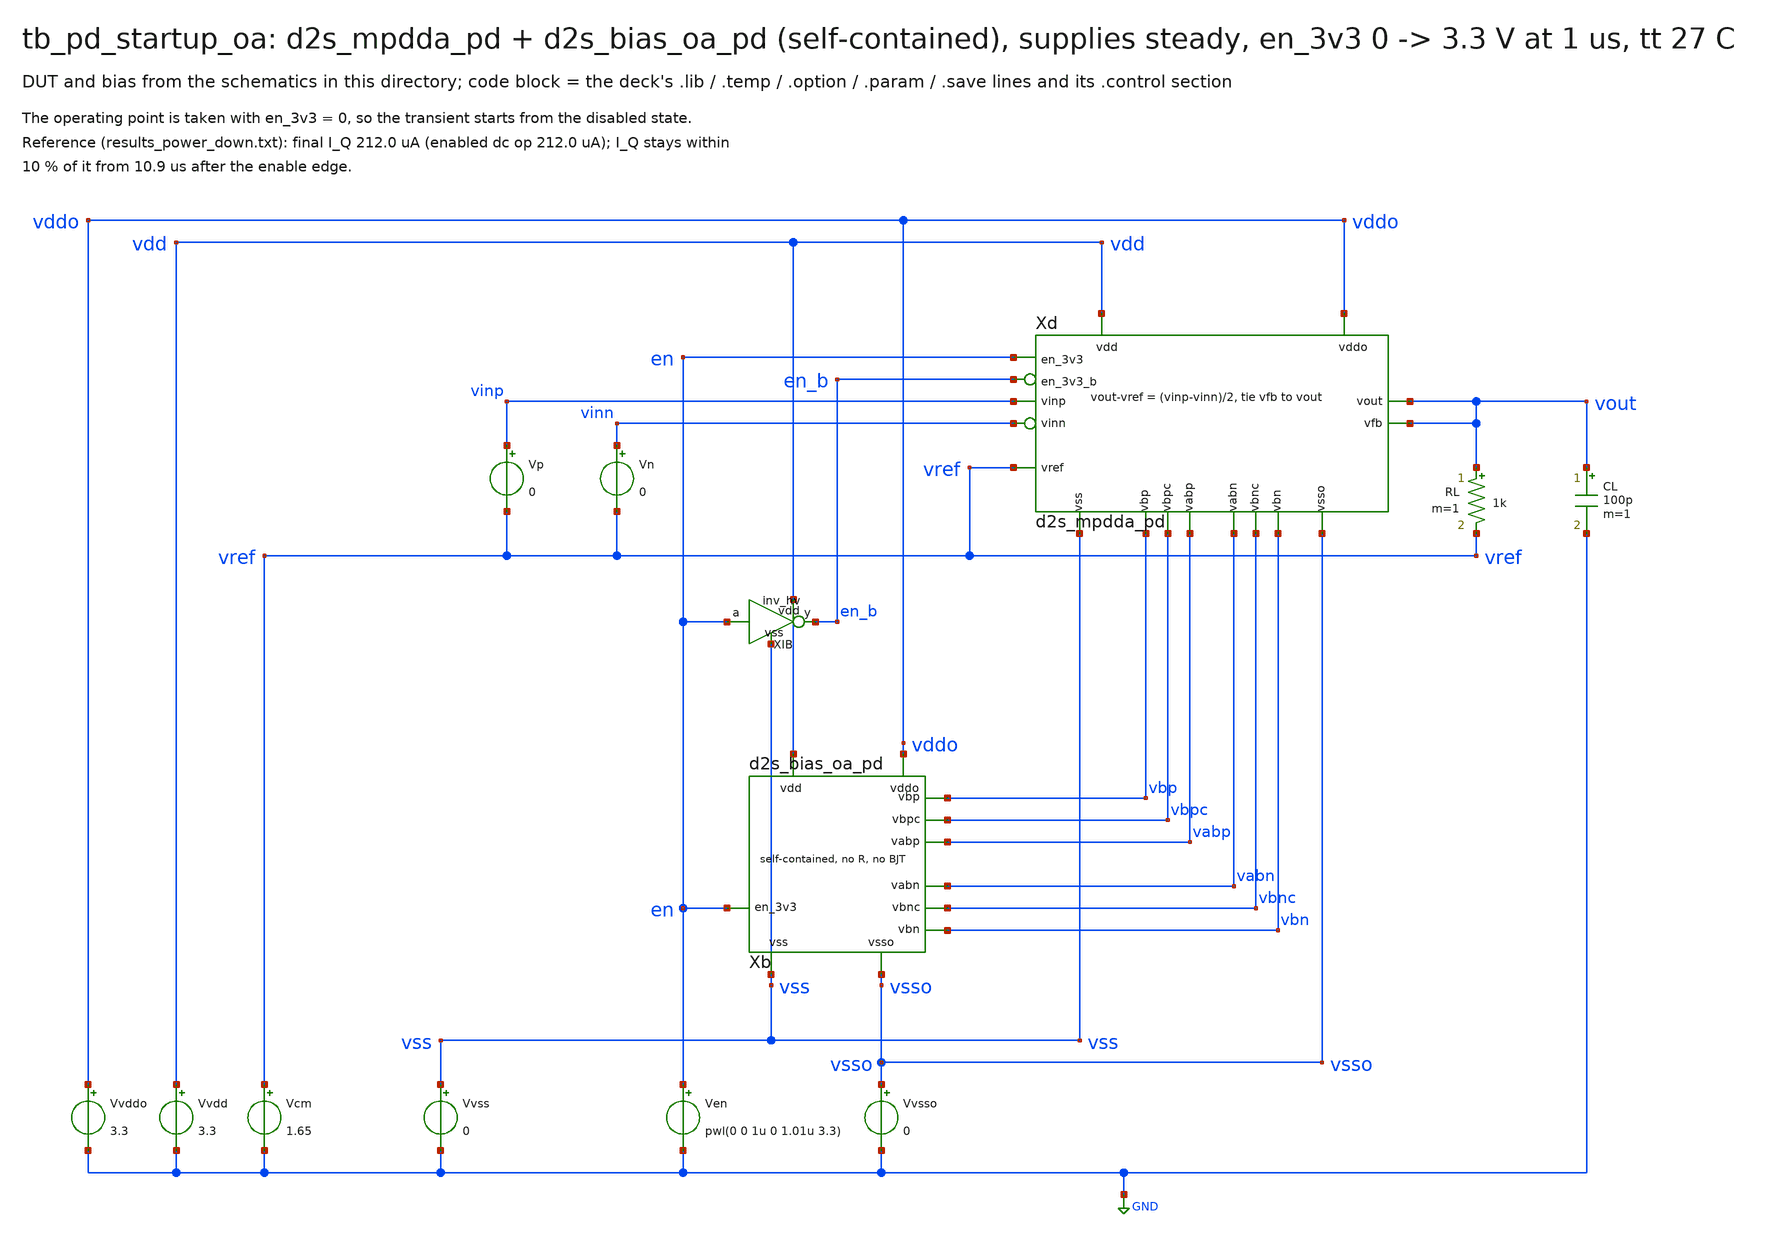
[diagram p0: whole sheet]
** sch_path: macros/sg13cmos5l_IOPadDiff2Single/testbenches/xschem/tb_pd_startup_oa.sch
**.subckt tb_pd_startup_oa
Vvdd vdd GND 3.3
Vvss vss GND 0
Vvddo vddo GND 3.3
Vvsso vsso GND 0
Ven en GND pwl(0 0 1u 0 1.01u 3.3)
Vcm vref GND 1.65
Xb vdd vss vddo vsso vbp vbn vbpc vbnc vabp vabn en d2s_bias_oa_pd
Xd vdd vss vddo vsso vinp vinn vref vout vout vbp vbn vbpc vbnc vabp vabn en en_b d2s_mpdda_pd
Vp vinp vref 0
Vn vinn vref 0
RL vout vref 1k m=1
CL vout GND 100p m=1
XIB vdd vss en en_b inv_hv
**** begin user architecture code

.lib cornerMOShv.lib mos_tt
.lib cornerRES.lib res_typ
.lib cornerCAP.lib cap_typ
.temp 27
.option method=gear
.save v(vout) v(en) @n.xd.xop.nsg13_hv_pmos[ids] v(xb.xc.vbr) v(xb.xc.ks)
.control
tran 20n 2m
let iq = abs(@n.xd.xop.nsg13_hv_pmos[ids])
meas tran iqf find iq at=2m
let hi = 1.1*iqf
let lo = 0.9*iqf
meas tran t1 when iq=hi cross=last
meas tran t2 when iq=lo cross=last
print iqf t1 t2
if $?batchmode = 0
  plot iq
  plot v(vout) v(xb.xc.vbr) v(xb.xc.ks) xlimit 0 50u
end
.endc

**** end user architecture code
**.ends

* expanding   symbol:  d2s_bias_oa_pd.sym # of pins=11
** sym_path: sudelbuecher/design_considerations/consolidation/bias_hierarchy_2026-10-27/before/macros/d2s_bias_oa_pd/schematic/xschem/d2s_bias_oa_pd.sym
** sch_path: sudelbuecher/design_considerations/consolidation/bias_hierarchy_2026-10-27/before/macros/d2s_bias_oa_pd/schematic/xschem/d2s_bias_oa_pd.sch
.subckt d2s_bias_oa_pd vdd vss vddo vsso vbp vbn vbpc vbnc vabp vabn en_3v3
*.iopin vdd
*.iopin vss
*.iopin vddo
*.iopin vsso
*.opin vbp
*.opin vbn
*.opin vbpc
*.opin vbnc
*.opin vabp
*.opin vabn
*.ipin en_3v3
XMS1 ks en_3v3_b vdd vdd sg13_hv_pmos w=0.5u l=100u ng=1 m=1 mm_ok=1
XMS2 ks vbr vss vss sg13_hv_nmos w=10u l=1u ng=1 m=1 mm_ok=1
XMS3 vpc ks vss vss sg13_hv_nmos w=0.5u l=2u ng=1 m=1 mm_ok=1
XP0 vpg vpg vdd vdd sg13_hv_pmos w=2u l=8u ng=1 m=1 mm_ok=1
XP0C vpc vpc vpg vdd sg13_hv_pmos w=0.5u l=2u ng=1 m=1 mm_ok=1
XMC10 vpc vbr d10 vss sg13_hv_nmos w=10u l=1u ng=1 m=1 mm_ok=1
XM10 d10 vnc vres vss sg13_hv_nmos w=180u l=1u ng=8 m=1 mm_ok=1
XMCL vres vbr vss vss sg13_hv_nmos w=3.4u l=30u ng=1 m=1 mm_ok=1
XP8 c8 vpg vdd vdd sg13_hv_pmos w=16u l=8u ng=8 m=1 mm_ok=1
XP8C vnc vpc c8 vdd sg13_hv_pmos w=4u l=2u ng=2 m=1 mm_ok=1
XM11 vnc vnc vss vss sg13_hv_nmos w=90u l=1u ng=4 m=1 mm_ok=1
XP2 c2 vpg vdd vdd sg13_hv_pmos w=4u l=8u ng=2 m=1 mm_ok=1
XP2C vbr vpc c2 vdd sg13_hv_pmos w=1u l=2u ng=1 m=1 mm_ok=1
XMCS vbr vbr vss vss sg13_hv_nmos w=3.4u l=30u ng=1 m=1 mm_ok=1
XPO co vpg vdd vdd sg13_hv_pmos w=40u l=8u ng=20 m=1 mm_ok=1
XPOC iref vpc co vdd sg13_hv_pmos w=10u l=2u ng=5 m=1 mm_ok=1
XNI ni ni vss vss sg13_hv_nmos w=6u l=6u ng=1 m=1 mm_ok=1
XBPC vbpc vbpc vdd vdd sg13_hv_pmos w=1u l=4u ng=1 m=1 mm_ok=1
XNBPC vbpc ni vss vss sg13_hv_nmos w=2.4u l=6u ng=1 m=1 mm_ok=1
XBP vbp vbp vdd vdd sg13_hv_pmos w=5u l=6u ng=1 m=1 mm_ok=1
XNBP vbp ni vss vss sg13_hv_nmos w=6u l=6u ng=1 m=1 mm_ok=1
XRP1 n1 n1 vddo vddo sg13_hv_pmos w=13.32u l=0.6u ng=2 m=1 mm_ok=1
XRP2 vabp vabp n1 vdd sg13_hv_pmos w=6.66u l=0.6u ng=1 m=1 mm_ok=1
XNABP vabp ni vss vss sg13_hv_nmos w=6u l=6u ng=1 m=1 mm_ok=1
XPBNC vbnc vbp vdd vdd sg13_hv_pmos w=2u l=6u ng=1 m=1 mm_ok=1
XBNC vbnc vbnc vss vss sg13_hv_nmos w=1u l=8u ng=1 m=1 mm_ok=1
XPBN vbn vbp vdd vdd sg13_hv_pmos w=5u l=6u ng=1 m=1 mm_ok=1
XBN vbn vbn vss vss sg13_hv_nmos w=6u l=6u ng=1 m=1 mm_ok=1
XPABN vabn vbp vdd vdd sg13_hv_pmos w=5u l=6u ng=1 m=1 mm_ok=1
XRN2 vabn vabn n2 vss sg13_hv_nmos w=4.4u l=1u ng=1 m=1 mm_ok=1
XRN1 n2 n2 vsso vsso sg13_hv_nmos w=8.8u l=1u ng=2 m=1 mm_ok=1
XSKS ks en_3v3_b vss vss sg13_hv_nmos w=1u l=0.45u ng=1 m=1 mm_ok=1
XSVPG vpg en_3v3 vdd vdd sg13_hv_pmos w=1u l=0.45u ng=1 m=1 mm_ok=1
XTDN ni en_3v3_b vss vss sg13_hv_nmos w=1u l=0.45u ng=1 m=1 mm_ok=1
XIP en_3v3_b en_3v3 vdd vdd sg13_hv_pmos w=1u l=0.45u ng=1 m=1 mm_ok=1
XIN en_3v3_b en_3v3 vss vss sg13_hv_nmos w=1u l=0.45u ng=1 m=1 mm_ok=1
XTGP ni en_3v3_b iref vdd sg13_hv_pmos w=1u l=0.45u ng=1 m=1 mm_ok=1
XTGN iref en_3v3 ni vss sg13_hv_nmos w=1u l=0.45u ng=1 m=1 mm_ok=1
.ends


* expanding   symbol:  d2s_mpdda_pd.sym # of pins=17
** sym_path: sudelbuecher/design_considerations/consolidation/bias_hierarchy_2026-10-27/before/macros/sg13cmos5l_IOPadDiff2Single/schematic/xschem/d2s_mpdda_pd.sym
** sch_path: sudelbuecher/design_considerations/consolidation/bias_hierarchy_2026-10-27/before/macros/sg13cmos5l_IOPadDiff2Single/schematic/xschem/d2s_mpdda_pd.sch
.subckt d2s_mpdda_pd vdd vss vddo vsso vinp vinn vref vout vfb vbp vbn vbpc vbnc vabp vabn en_3v3
+ en_3v3_b
*.iopin vdd
*.iopin vss
*.iopin vddo
*.iopin vsso
*.ipin vinp
*.ipin vinn
*.ipin vref
*.iopin vout
*.ipin vfb
*.ipin vbp
*.ipin vbn
*.ipin vbpc
*.ipin vbnc
*.ipin vabp
*.ipin vabn
*.ipin en_3v3
*.ipin en_3v3_b
XA x y vinp vref vdd vss vbp unit_r2
XB x y vref vinn vdd vss vbp unit_r2
XC1 x y vref vfb vdd vss vbp unit_r2
XC2 x y vref vfb vdd vss vbp unit_r2
XFNL l2 vabn l1 vss sg13_hv_nmos w=4.4u l=1u ng=1 m=1 mm_ok=1
XCX l1 vbnc x vss sg13_hv_nmos w=30u l=3u ng=2 m=1 mm_ok=1
XSX x vbn vss vss sg13_hv_nmos w=36u l=6u ng=4 m=1 mm_ok=1
XPL pl l2 vdd vdd sg13_hv_pmos w=24u l=4u ng=4 m=1 mm_ok=1
XPCL l2 vbpc pl vdd sg13_hv_pmos w=30u l=3u ng=2 m=1 mm_ok=1
XFPL l1 vabp l2 vdd sg13_hv_pmos w=6.66u l=0.6u ng=1 m=1 mm_ok=1
XPR pr l2 vdd vdd sg13_hv_pmos w=24u l=4u ng=4 m=1 mm_ok=1
XPCR a vbpc pr vdd sg13_hv_pmos w=30u l=3u ng=2 m=1 mm_ok=1
XABP b vabp a vdd sg13_hv_pmos w=6.66u l=0.6u ng=1 m=1 mm_ok=1
XABN a vabn b vss sg13_hv_nmos w=4.4u l=1u ng=1 m=1 mm_ok=1
XCY b vbnc y vss sg13_hv_nmos w=30u l=3u ng=2 m=1 mm_ok=1
XSY y vbn vss vss sg13_hv_nmos w=36u l=6u ng=4 m=1 mm_ok=1
XOP vout a vddo vddo sg13_hv_pmos w=546.12u l=0.6u ng=82 m=1 mm_ok=1
XON vout b vsso vsso sg13_hv_nmos w=299.2u l=1u ng=68 m=1 mm_ok=1
XCMA vout a vout vout sg13_hv_pmos w=16u l=16u ng=1 m=1 mm_ok=1
XCMB b vout b b sg13_hv_pmos w=16u l=16u ng=1 m=1 mm_ok=1
XSABP vabp en_3v3 vdd vdd sg13_hv_pmos w=1u l=0.45u ng=1 m=1 mm_ok=1
XSA a en_3v3 vddo vddo sg13_hv_pmos w=1u l=0.45u ng=1 m=1 mm_ok=1
XSABN vabn en_3v3_b vss vss sg13_hv_nmos w=1u l=0.45u ng=1 m=1 mm_ok=1
XSB b en_3v3_b vsso vsso sg13_hv_nmos w=1u l=0.45u ng=1 m=1 mm_ok=1
.ends


* expanding   symbol:  inv_hv.sym # of pins=4
** sym_path: macros/hv_logic/schematic/xschem/inv_hv.sym
** sch_path: macros/hv_logic/schematic/xschem/inv_hv.sch
.subckt inv_hv vdd vss a y
*.iopin vdd
*.iopin vss
*.ipin a
*.opin y
XP y a vdd vdd sg13_hv_pmos w=1u l=0.45u ng=1 m=1 mm_ok=1
XN y a vss vss sg13_hv_nmos w=1u l=0.45u ng=1 m=1 mm_ok=1
.ends


* expanding   symbol:  unit_r2.sym # of pins=7
** sym_path: sudelbuecher/design_considerations/class_ab_pad_driver/improvements/xschem/unit_r2.sym
** sch_path: sudelbuecher/design_considerations/class_ab_pad_driver/improvements/xschem/unit_r2.sch
.subckt unit_r2 x y gp gn vdd vss vbp
*.opin x
*.opin y
*.ipin gp
*.ipin gn
*.iopin vdd
*.iopin vss
*.ipin vbp
XTa sa vbp vdd vdd sg13_hv_pmos w=5u l=6u ng=1 m=1 mm_ok=1
XTb sb vbp vdd vdd sg13_hv_pmos w=5u l=6u ng=1 m=1 mm_ok=1
XMa y gp sa sa sg13_hv_pmos w=20u l=1u ng=2 m=1 mm_ok=1
XMb x gn sb sb sg13_hv_pmos w=20u l=1u ng=2 m=1 mm_ok=1
XR sa sb vss rhigh w=0.5u l=50.6u m=1 b=0 mm_ok=1
.ends

.GLOBAL GND
.end
